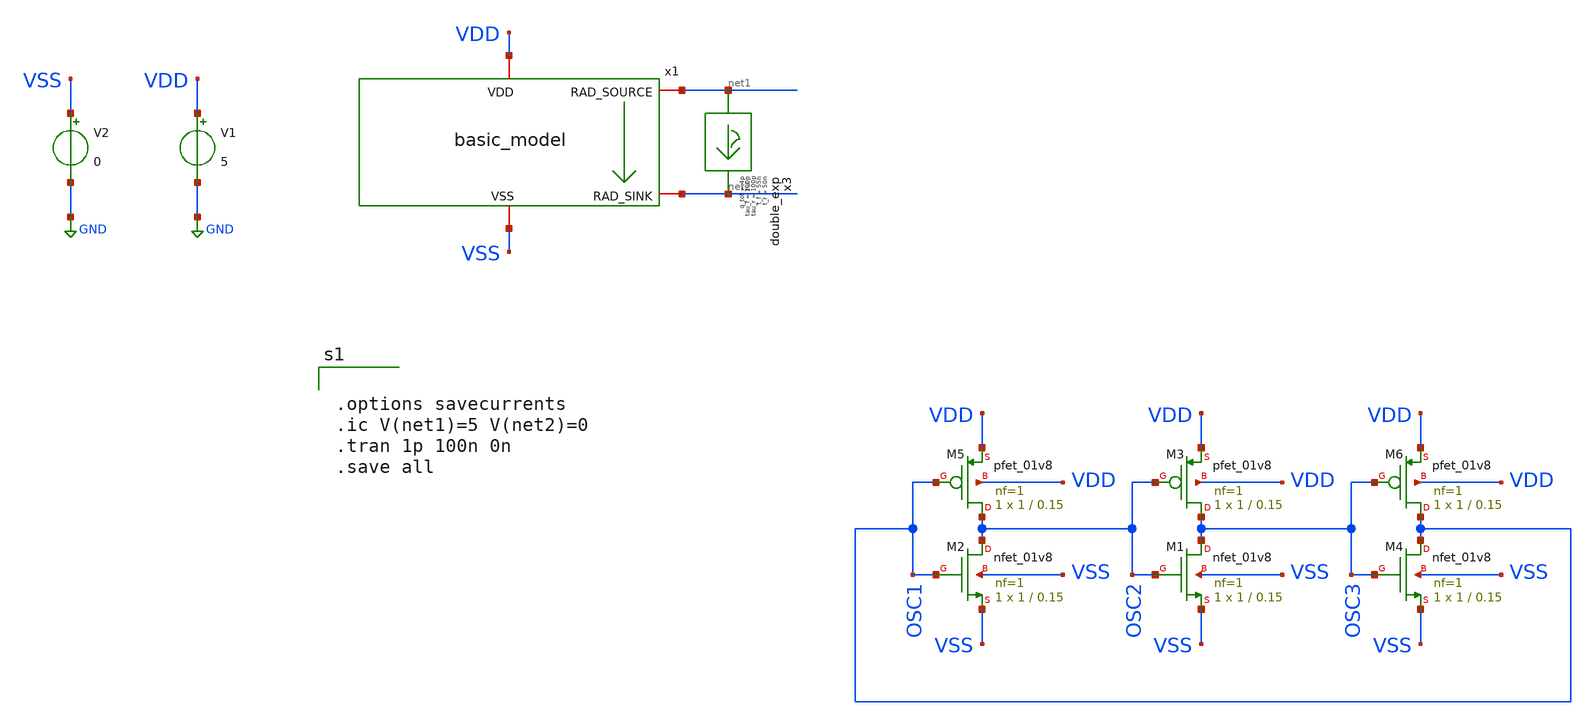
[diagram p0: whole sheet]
** sch_path: untitled-4.sch
**.subckt untitled-4
V1 VDD GND 5
V2 VSS GND 0
x3 net1 net2 double_exp t_r=50n tau_r=100p t_f=55n tau_f=100p q_tot=4p
x1 VDD net1 net2 VSS basic_model IS_N=1e-18 BF_N=100 VAF_N=50 IKF_N=0.01 CJE_N=0.2p CJC_N=0.1p
+ TF_N=0.2n TR_N=2n IS_P=1e-18 BF_P=100 VAF_P=50 IKF_P=0.01 CJE_P=0.3p CJC_P=0.15p TF_P=0.3n TR_P=3n
XM2 OSC2 OSC1 VSS VSS sky130_fd_pr__nfet_01v8 L=0.15 W=1 nf=1 ad='int((nf+1)/2) * W/nf * 0.29' as='int((nf+2)/2) * W/nf * 0.29'
+ pd='2*int((nf+1)/2) * (W/nf + 0.29)' ps='2*int((nf+2)/2) * (W/nf + 0.29)' nrd='0.29 / W' nrs='0.29 / W'
+ sa=0 sb=0 sd=0 mult=1 m=1
XM5 OSC2 OSC1 VDD VDD sky130_fd_pr__pfet_01v8 L=0.15 W=1 nf=1 ad='int((nf+1)/2) * W/nf * 0.29' as='int((nf+2)/2) * W/nf * 0.29'
+ pd='2*int((nf+1)/2) * (W/nf + 0.29)' ps='2*int((nf+2)/2) * (W/nf + 0.29)' nrd='0.29 / W' nrs='0.29 / W'
+ sa=0 sb=0 sd=0 mult=1 m=1
XM1 OSC3 OSC2 VSS VSS sky130_fd_pr__nfet_01v8 L=0.15 W=1 nf=1 ad='int((nf+1)/2) * W/nf * 0.29' as='int((nf+2)/2) * W/nf * 0.29'
+ pd='2*int((nf+1)/2) * (W/nf + 0.29)' ps='2*int((nf+2)/2) * (W/nf + 0.29)' nrd='0.29 / W' nrs='0.29 / W'
+ sa=0 sb=0 sd=0 mult=1 m=1
XM3 OSC3 OSC2 VDD VDD sky130_fd_pr__pfet_01v8 L=0.15 W=1 nf=1 ad='int((nf+1)/2) * W/nf * 0.29' as='int((nf+2)/2) * W/nf * 0.29'
+ pd='2*int((nf+1)/2) * (W/nf + 0.29)' ps='2*int((nf+2)/2) * (W/nf + 0.29)' nrd='0.29 / W' nrs='0.29 / W'
+ sa=0 sb=0 sd=0 mult=1 m=1
XM4 OSC1 OSC3 VSS VSS sky130_fd_pr__nfet_01v8 L=0.15 W=1 nf=1 ad='int((nf+1)/2) * W/nf * 0.29' as='int((nf+2)/2) * W/nf * 0.29'
+ pd='2*int((nf+1)/2) * (W/nf + 0.29)' ps='2*int((nf+2)/2) * (W/nf + 0.29)' nrd='0.29 / W' nrs='0.29 / W'
+ sa=0 sb=0 sd=0 mult=1 m=1
XM6 OSC1 OSC3 VDD VDD sky130_fd_pr__pfet_01v8 L=0.15 W=1 nf=1 ad='int((nf+1)/2) * W/nf * 0.29' as='int((nf+2)/2) * W/nf * 0.29'
+ pd='2*int((nf+1)/2) * (W/nf + 0.29)' ps='2*int((nf+2)/2) * (W/nf + 0.29)' nrd='0.29 / W' nrs='0.29 / W'
+ sa=0 sb=0 sd=0 mult=1 m=1
**** begin user architecture code


.options savecurrents
.ic V(net1)=5 V(net2)=0
.tran 1p 100n 0n
.save all




.include /usr/local/share/rad_modeling_blocks/rad_modeling_blocks.spice



** opencircuitdesign pdks install
.lib $::SKYWATER_MODELS/sky130.lib.spice tt


**** end user architecture code
**.ends

* expanding   symbol:  double_exp.sym # of pins=2
** sym_path: xschem_rad_library/double_exp.sym
** sch_path: xschem_rad_library/double_exp.sch
.subckt double_exp in out  t_r=0 t_f=0 tau_r=0 tau_f=0 q_tot=0
*.opin OUT
*.ipin IN
I1 IN OUT EXP(0 {q_tot / (t_f-t_r+tau_f-tau_r)} {t_r} {tau_r} {t_f} {tau_f})
.ends


* expanding   symbol:  OSCRE/latchup/basic_model.sym # of pins=4
** sym_path: latchup/basic_model.sym
** sch_path: latchup/basic_model.sch
.subckt basic_model VDD RAD_SOURCE RAD_SINK VSS   IS_N=1e-16  BF_N=100  VAF_N=100  IKF_N=0.1
+  CJE_N=2p  CJC_N=2p  TF_N=0.1n  TR_N=10n  IS_P=1e-16  BF_P=100  VAF_P=100  IKF_P=0.1  CJE_P=2p  CJC_P=2p
+  TF_P=0.1n  TR_P=10n
*.iopin VDD
*.iopin VSS
*.iopin RAD_SOURCE
*.iopin RAD_SINK
Q1 RAD_SINK RAD_SOURCE VDD pnp_cust area=1 m=1
Q2 RAD_SOURCE RAD_SINK VSS npn_cust area=1 m=1
R3 RAD_SINK VSS 50 m=1
R4 VDD RAD_SOURCE 50 m=1
**** begin user architecture code


.model npn_cust npn (IS={IS_N} BF={BF_N} VAF={VAF_N} IKF={IKF_N} CJE={CJE_N} CJC={CJC_N} TF={TF_N} TR={TR_N})
.model pnp_cust pnp (IS=1e-16 BF=100 VAF=100 IKF=0.1 CJE=2p CJC=2p TF=0.1n TR=10n)


**** end user architecture code
.ends

.GLOBAL GND
.end
